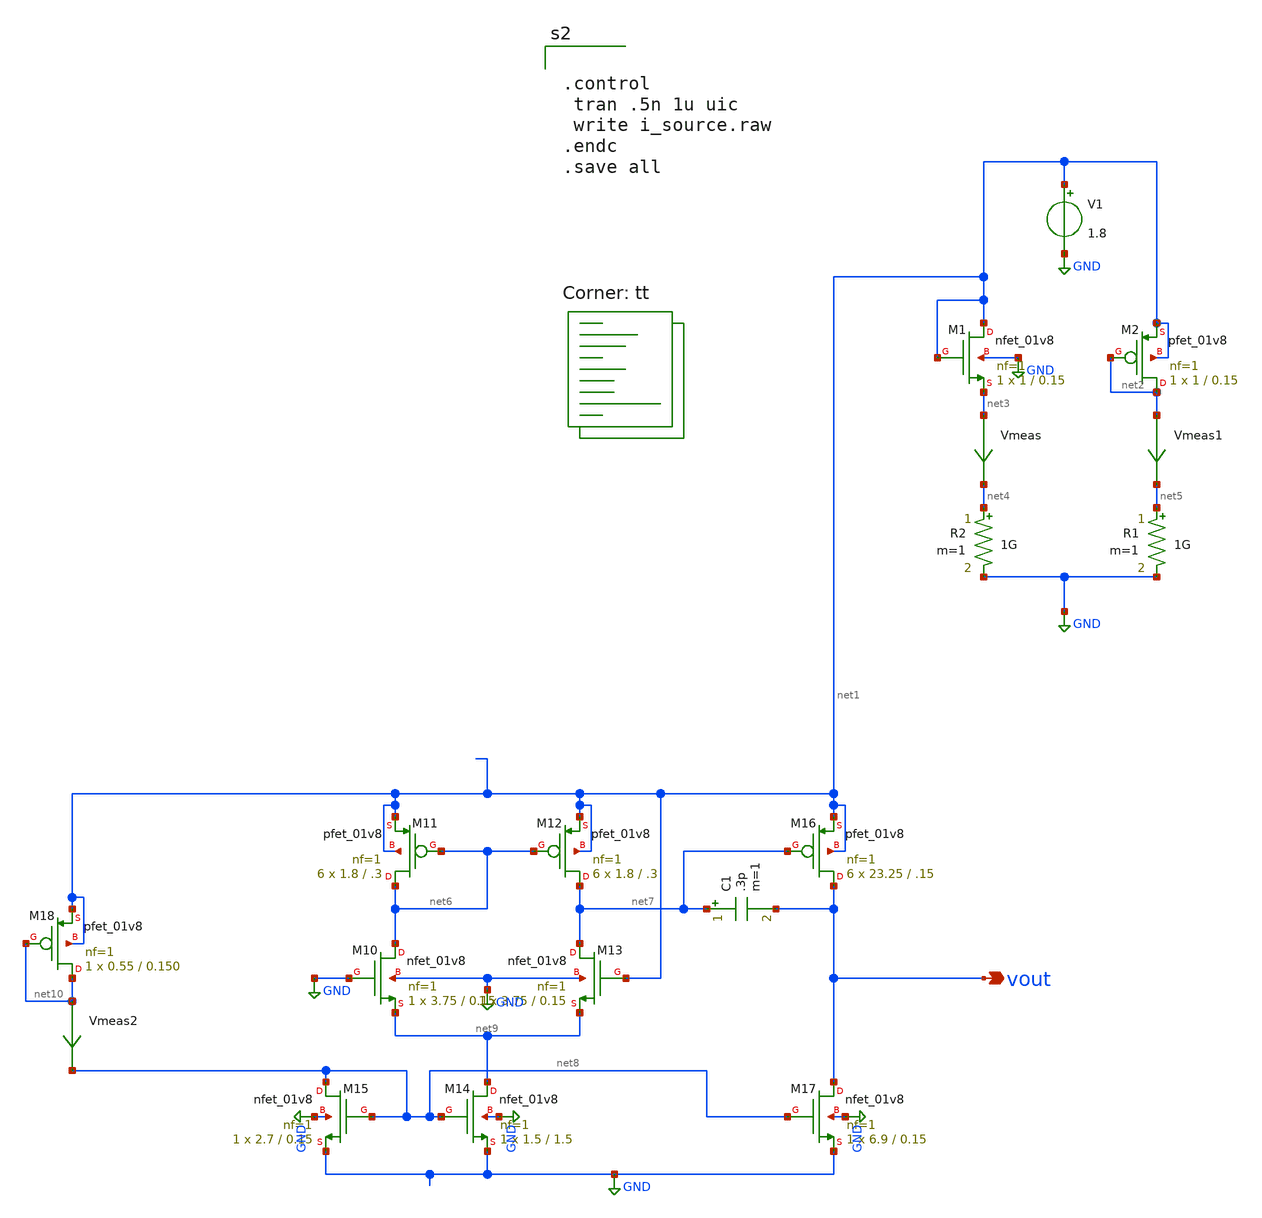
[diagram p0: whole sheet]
** sch_path: designs/prubs/i_source.sch
**.subckt i_source vout
*.opin vout
XM1 net1 net1 net3 GND sky130_fd_pr__nfet_01v8 L=0.15 W=1 nf=1 ad='int((nf+1)/2) * W/nf * 0.29' as='int((nf+2)/2) * W/nf * 0.29'
+ pd='2*int((nf+1)/2) * (W/nf + 0.29)' ps='2*int((nf+2)/2) * (W/nf + 0.29)' nrd='0.29 / W' nrs='0.29 / W'
+ sa=0 sb=0 sd=0 mult=1 m=1
Vmeas net3 net4 0
.save i(vmeas)
Vmeas1 net2 net5 0
.save i(vmeas1)
XM2 net2 net2 net1 net1 sky130_fd_pr__pfet_01v8 L=0.15 W=1 nf=1 ad='int((nf+1)/2) * W/nf * 0.29' as='int((nf+2)/2) * W/nf * 0.29'
+ pd='2*int((nf+1)/2) * (W/nf + 0.29)' ps='2*int((nf+2)/2) * (W/nf + 0.29)' nrd='0.29 / W' nrs='0.29 / W'
+ sa=0 sb=0 sd=0 mult=1 m=1
V1 net1 GND 1.8
R1 net5 GND 1G m=1
R2 net4 GND 1G m=1
Vmeas2 net10 net8 0
.save i(vmeas2)
XM10 net6 GND net9 GND sky130_fd_pr__nfet_01v8 L=0.15 W=3.75 nf=1 ad='int((1 + 1)/2) * 3.75 / 1 * 0.29'
+ as='int((1 + 2)/2) * 3.75 / 1 * 0.29' pd='2*int((1 + 1)/2) * (3.75 / 1 + 0.29)' ps='2*int((1 + 2)/2) * (3.75 / 1 + 0.29)'
+ nrd='0.29 / 3.75 ' nrs='0.29 / 3.75 ' sa=0 sb=0 sd=0 mult=1 m=1
XM11 net6 net6 net1 net1 sky130_fd_pr__pfet_01v8 L=.3 W=1.8 nf=1 ad='int((nf+1)/2) * W/nf * 0.29' as='int((nf+2)/2) * W/nf * 0.29'
+ pd='2*int((nf+1)/2) * (W/nf + 0.29)' ps='2*int((nf+2)/2) * (W/nf + 0.29)' nrd='0.29 / W' nrs='0.29 / W'
+ sa=0 sb=0 sd=0 mult=6 m=6
XM12 net7 net6 net1 net1 sky130_fd_pr__pfet_01v8 L=.3 W=1.8 nf=1 ad='int((nf+1)/2) * W/nf * 0.29' as='int((nf+2)/2) * W/nf * 0.29'
+ pd='2*int((nf+1)/2) * (W/nf + 0.29)' ps='2*int((nf+2)/2) * (W/nf + 0.29)' nrd='0.29 / W' nrs='0.29 / W'
+ sa=0 sb=0 sd=0 mult=6 m=6
XM13 net7 net1 net9 GND sky130_fd_pr__nfet_01v8 L=0.15 W=3.75 nf=1 ad='int((1 + 1)/2) * 3.75 / 1 * 0.29'
+ as='int((1 + 2)/2) * 3.75 / 1 * 0.29' pd='2*int((1 + 1)/2) * (3.75 / 1 + 0.29)' ps='2*int((1 + 2)/2) * (3.75 / 1 + 0.29)'
+ nrd='0.29 / 3.75 ' nrs='0.29 / 3.75 ' sa=0 sb=0 sd=0 mult=1 m=1
XM14 net9 net8 GND GND sky130_fd_pr__nfet_01v8 L=1.5 W=1.5 nf=1 ad='int((1 + 1)/2) * 1.5 / 1 * 0.29'
+ as='int((1 + 2)/2) * 1.5 / 1 * 0.29' pd='2*int((1 + 1)/2) * (1.5 / 1 + 0.29)' ps='2*int((1 + 2)/2) * (1.5 / 1 + 0.29)'
+ nrd='0.29 / 1.5 ' nrs='0.29 / 1.5 ' sa=0 sb=0 sd=0 mult=1 m=1
XM15 net8 net8 GND GND sky130_fd_pr__nfet_01v8 L=0.15 W=2.7 nf=1 ad='int((1 + 1)/2) * 2.7 / 1 * 0.29'
+ as='int((1 + 2)/2) * 2.7 / 1 * 0.29' pd='2*int((1 + 1)/2) * (2.7 / 1 + 0.29)' ps='2*int((1 + 2)/2) * (2.7 / 1 + 0.29)'
+ nrd='0.29 / 2.7 ' nrs='0.29 / 2.7 ' sa=0 sb=0 sd=0 mult=1 m=1
XM16 vout net7 net1 net1 sky130_fd_pr__pfet_01v8 L=.15 W=23.25 nf=1 ad='int((nf+1)/2) * W/nf * 0.29'
+ as='int((nf+2)/2) * W/nf * 0.29' pd='2*int((nf+1)/2) * (W/nf + 0.29)' ps='2*int((nf+2)/2) * (W/nf + 0.29)'
+ nrd='0.29 / W' nrs='0.29 / W' sa=0 sb=0 sd=0 mult=6 m=6
C1 net7 vout .3p m=1
XM17 vout net8 GND GND sky130_fd_pr__nfet_01v8 L=0.15 W=6.9 nf=1 ad='int((1 + 1)/2) * 6.9 / 1 * 0.29'
+ as='int((1 + 2)/2) * 6.9 / 1 * 0.29' pd='2*int((1 + 1)/2) * (6.9 / 1 + 0.29)' ps='2*int((1 + 2)/2) * (6.9 / 1 + 0.29)'
+ nrd='0.29 / 6.9 ' nrs='0.29 / 6.9 ' sa=0 sb=0 sd=0 mult=1 m=1
XM18 net10 net10 net1 net1 sky130_fd_pr__pfet_01v8 L=0.150 W=0.55 nf=1 ad='int((nf+1)/2) * W/nf * 0.29'
+ as='int((nf+2)/2) * W/nf * 0.29' pd='2*int((nf+1)/2) * (W/nf + 0.29)' ps='2*int((nf+2)/2) * (W/nf + 0.29)'
+ nrd='0.29 / W' nrs='0.29 / W' sa=0 sb=0 sd=0 mult=1 m=1
**** begin user architecture code


.control
 tran .5n 1u uic
 write i_source.raw
.endc
.save all


.lib $::SKYWATER_MODELS/sky130.lib.spice tt
**** end user architecture code
**.ends
.GLOBAL GND
.end
